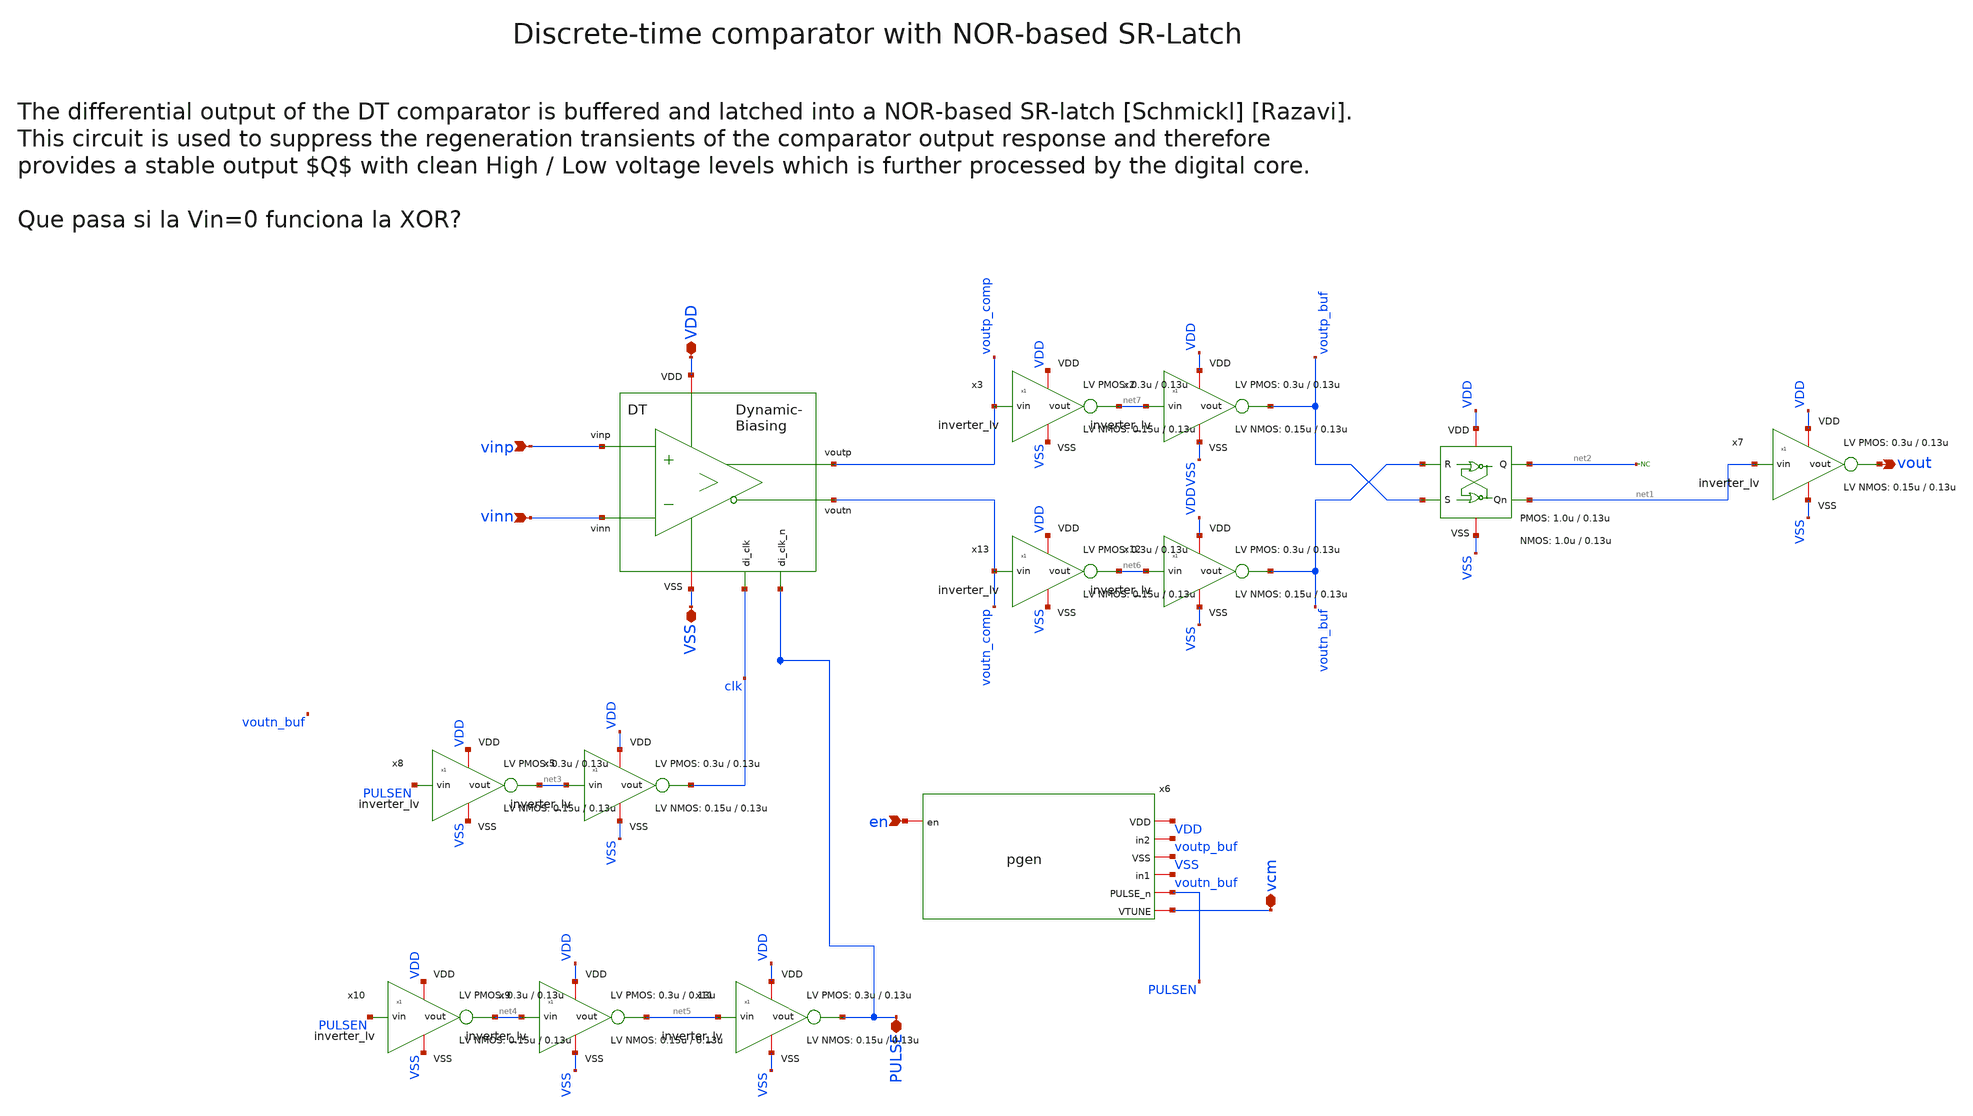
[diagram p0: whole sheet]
** sch_path: xschem/comparator/discrete_time/DT_comparator.sch
**.subckt DT_comparator VDD vout VSS vinp vinn en PULSE vcm
*.iopin VDD
*.opin vout
*.iopin VSS
*.ipin vinp
*.ipin vinn
*.ipin en
*.iopin PULSE
*.iopin vcm
x5 VDD net3 clk VSS inverter_lv W_P=0.3u L_P=0.13u W_N=0.15u L_N=0.13u N_C=1
* noconn #net2
x4 VDD voutp_buf net1 VSS net2 voutn_buf SR_latch W_P_SR=1.0u L_P_SR=0.13u W_N_SR=1.0u L_N_SR=0.13u
x6 VDD voutp_buf VSS voutn_buf PULSEN vcm en pgen
x1 PULSE clk VDD voutp_comp vinp VSS voutn_comp vinn dynamic_biasing_comparator
x8 VDD PULSEN net3 VSS inverter_lv W_P=0.3u L_P=0.13u W_N=0.15u L_N=0.13u N_C=1
x9 VDD net4 net5 VSS inverter_lv W_P=0.3u L_P=0.13u W_N=0.15u L_N=0.13u N_C=1
x10 VDD PULSEN net4 VSS inverter_lv W_P=0.3u L_P=0.13u W_N=0.15u L_N=0.13u N_C=1
x11 VDD net5 PULSE VSS inverter_lv W_P=0.3u L_P=0.13u W_N=0.15u L_N=0.13u N_C=1
x12 VDD net6 voutn_buf VSS inverter_lv W_P=0.3u L_P=0.13u W_N=0.15u L_N=0.13u N_C=1
x13 VDD voutn_comp net6 VSS inverter_lv W_P=0.3u L_P=0.13u W_N=0.15u L_N=0.13u N_C=1
x2 VDD net7 voutp_buf VSS inverter_lv W_P=0.3u L_P=0.13u W_N=0.15u L_N=0.13u N_C=1
x3 VDD voutp_comp net7 VSS inverter_lv W_P=0.3u L_P=0.13u W_N=0.15u L_N=0.13u N_C=1
x7 VDD net1 vout VSS inverter_lv W_P=0.3u L_P=0.13u W_N=0.15u L_N=0.13u N_C=1
**.ends
.end
